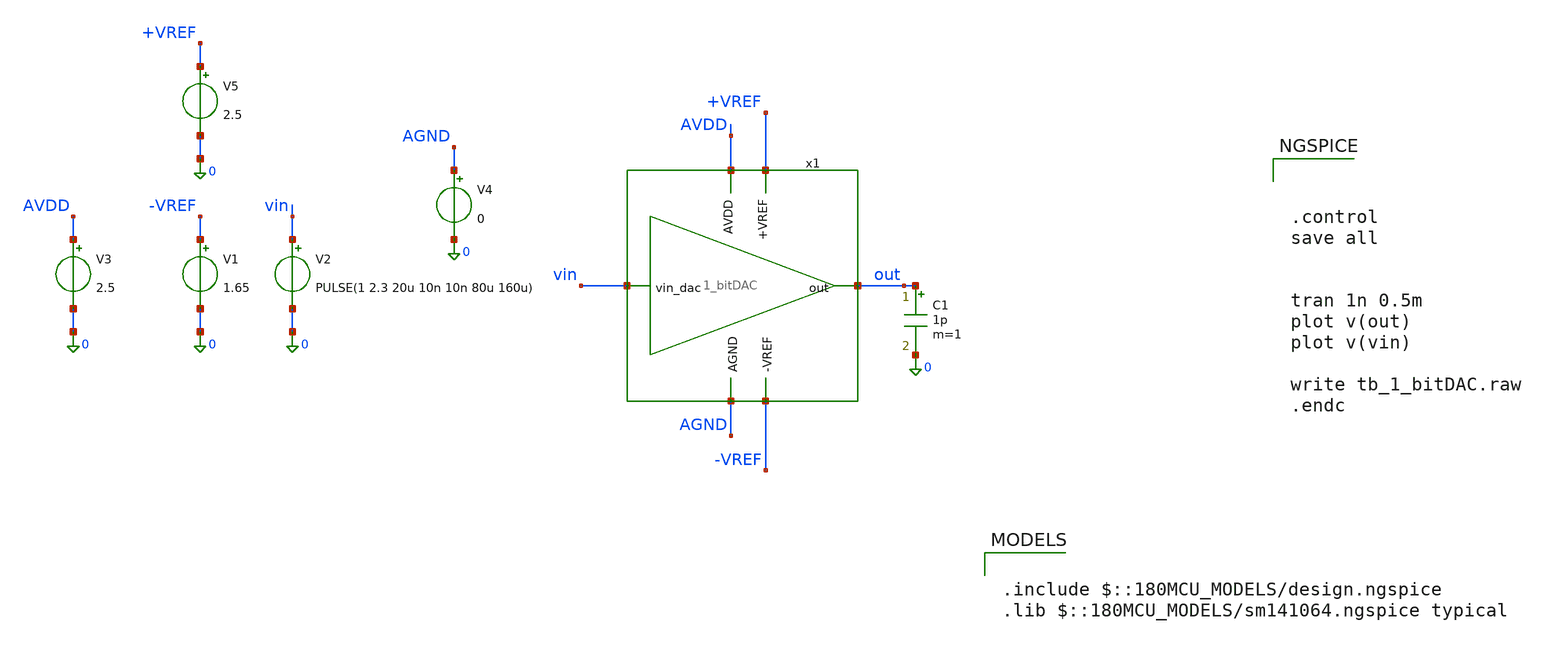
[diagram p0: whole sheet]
** sch_path: amplifier/tb_1_bitDAC.sch
**.subckt tb_1_bitDAC
V2 vin 0 PULSE(1 2.3 20u 10n 10n 80u 160u)
V3 AVDD 0 2.5
V1 -VREF 0 1.65
x1 AVDD +VREF vin out AGND -VREF 1_bitDAC
C1 out 0 1p m=1
V4 AGND 0 0
V5 +VREF 0 2.5
**** begin user architecture code

.include $::180MCU_MODELS/design.ngspice
.lib $::180MCU_MODELS/sm141064.ngspice typical




.control
save all


tran 1n 0.5m
plot v(out)
plot v(vin)

write tb_1_bitDAC.raw
.endc


**** end user architecture code
**.ends

* expanding   symbol:  1_bitDAC.sym # of pins=6
** sym_path: amplifier/1_bitDAC.sym
** sch_path: amplifier/1_bitDAC.sch
.subckt 1_bitDAC AVDD +VREF vin_dac out AGND -VREF
*.ipin vin_dac
*.opin out
*.ipin AVDD
*.ipin AGND
*.ipin +VREF
*.ipin -VREF
XM7 net1 vin_dac AGND AGND nfet_03v3 L=350n W=5u nf=1 ad='int((nf+1)/2) * W/nf * 0.18u' as='int((nf+2)/2) * W/nf * 0.18u'
+ pd='2*int((nf+1)/2) * (W/nf + 0.18u)' ps='2*int((nf+2)/2) * (W/nf + 0.18u)' nrd='0.18u / W' nrs='0.18u / W'
+ sa=0 sb=0 sd=0 m=1
XM9 net1 vin_dac AVDD AVDD pfet_03v3 L=350n W=10u nf=1 ad='int((nf+1)/2) * W/nf * 0.18u' as='int((nf+2)/2) * W/nf * 0.18u'
+ pd='2*int((nf+1)/2) * (W/nf + 0.18u)' ps='2*int((nf+2)/2) * (W/nf + 0.18u)' nrd='0.18u / W' nrs='0.18u / W'
+ sa=0 sb=0 sd=0 m=1
XM1 out net1 +VREF +VREF pfet_03v3 L=350n W=20u nf=1 ad='int((nf+1)/2) * W/nf * 0.18u' as='int((nf+2)/2) * W/nf * 0.18u'
+ pd='2*int((nf+1)/2) * (W/nf + 0.18u)' ps='2*int((nf+2)/2) * (W/nf + 0.18u)' nrd='0.18u / W' nrs='0.18u / W'
+ sa=0 sb=0 sd=0 m=1
XM2 +VREF vin_dac out AGND nfet_03v3 L=350n W=10u nf=1 ad='int((nf+1)/2) * W/nf * 0.18u' as='int((nf+2)/2) * W/nf * 0.18u'
+ pd='2*int((nf+1)/2) * (W/nf + 0.18u)' ps='2*int((nf+2)/2) * (W/nf + 0.18u)' nrd='0.18u / W' nrs='0.18u / W'
+ sa=0 sb=0 sd=0 m=1
XM3 out net1 -VREF -VREF nfet_03v3 L=350n W=20u nf=1 ad='int((nf+1)/2) * W/nf * 0.18u' as='int((nf+2)/2) * W/nf * 0.18u'
+ pd='2*int((nf+1)/2) * (W/nf + 0.18u)' ps='2*int((nf+2)/2) * (W/nf + 0.18u)' nrd='0.18u / W' nrs='0.18u / W'
+ sa=0 sb=0 sd=0 m=1
XM4 -VREF vin_dac out AVDD pfet_03v3 L=350n W=10u nf=1 ad='int((nf+1)/2) * W/nf * 0.18u' as='int((nf+2)/2) * W/nf * 0.18u'
+ pd='2*int((nf+1)/2) * (W/nf + 0.18u)' ps='2*int((nf+2)/2) * (W/nf + 0.18u)' nrd='0.18u / W' nrs='0.18u / W'
+ sa=0 sb=0 sd=0 m=1
.ends

.end
